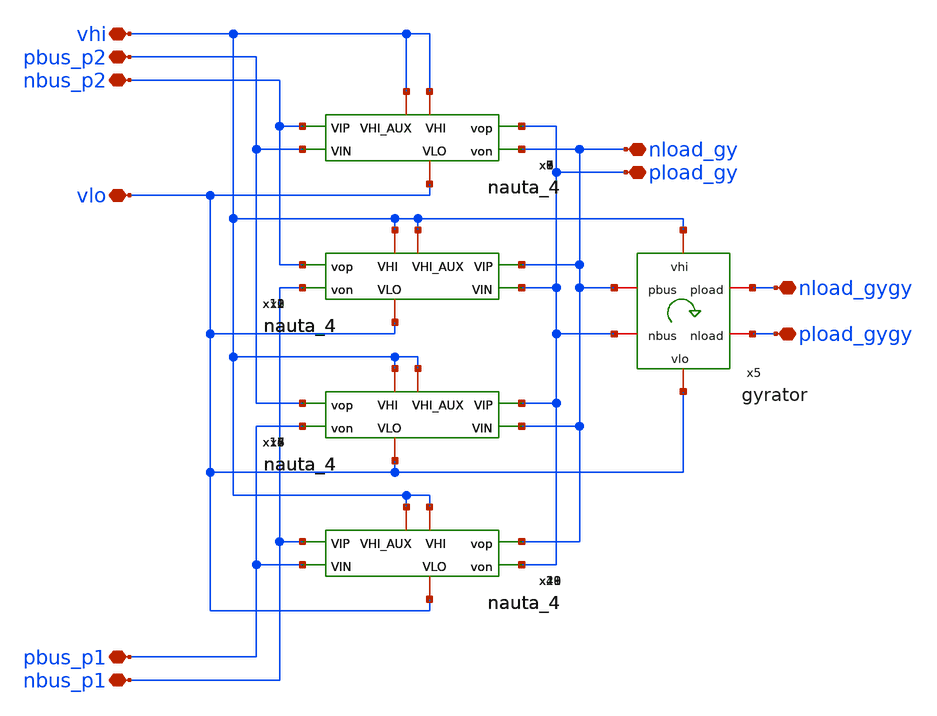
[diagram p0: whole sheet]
** sch_path: xschem/floater.sch
**.subckt floater nbus_p1 pbus_p1 nbus_p2 pbus_p2 vhi vlo pload_gy nload_gy pload_gygy nload_gygy
*.iopin nbus_p1
*.iopin pbus_p1
*.iopin nbus_p2
*.iopin pbus_p2
*.iopin vhi
*.iopin vlo
*.iopin pload_gy
*.iopin nload_gy
*.iopin pload_gygy
*.iopin nload_gygy
x1 vhi vhi nbus_p2 pload_gy pbus_p2 nload_gy vlo nauta_4
x2 vhi vhi nload_gy nbus_p2 pload_gy nbus_p1 vlo nauta_4
x3 vhi vhi pload_gy pbus_p2 nload_gy pbus_p1 vlo nauta_4
x4 vhi vhi nbus_p1 nload_gy pbus_p1 pload_gy vlo nauta_4
x5 vhi nload_gygy nload_gy pload_gygy pload_gy vlo gyrator
x6 vhi vhi nbus_p2 pload_gy pbus_p2 nload_gy vlo nauta_4
x7 vhi vhi nbus_p2 pload_gy pbus_p2 nload_gy vlo nauta_4
x8 vhi vhi nbus_p2 pload_gy pbus_p2 nload_gy vlo nauta_4
x9 vhi vhi nbus_p2 pload_gy pbus_p2 nload_gy vlo nauta_4
x10 vhi vhi nload_gy nbus_p2 pload_gy nbus_p1 vlo nauta_4
x11 vhi vhi nload_gy nbus_p2 pload_gy nbus_p1 vlo nauta_4
x12 vhi vhi nload_gy nbus_p2 pload_gy nbus_p1 vlo nauta_4
x13 vhi vhi nload_gy nbus_p2 pload_gy nbus_p1 vlo nauta_4
x14 vhi vhi pload_gy pbus_p2 nload_gy pbus_p1 vlo nauta_4
x15 vhi vhi pload_gy pbus_p2 nload_gy pbus_p1 vlo nauta_4
x16 vhi vhi pload_gy pbus_p2 nload_gy pbus_p1 vlo nauta_4
x17 vhi vhi pload_gy pbus_p2 nload_gy pbus_p1 vlo nauta_4
x18 vhi vhi nbus_p1 nload_gy pbus_p1 pload_gy vlo nauta_4
x19 vhi vhi nbus_p1 nload_gy pbus_p1 pload_gy vlo nauta_4
x20 vhi vhi nbus_p1 nload_gy pbus_p1 pload_gy vlo nauta_4
x21 vhi vhi nbus_p1 nload_gy pbus_p1 pload_gy vlo nauta_4
**.ends

* expanding   symbol:  nauta_4.sym # of pins=7
** sym_path: xschem/nauta_4.sym
** sch_path: xschem/nauta_4.sch
.subckt nauta_4 VHI_AUX VHI VIP vop VIN von VLO
*.ipin VIP
*.ipin VIN
*.opin vop
*.opin von
*.iopin VHI
*.iopin VHI_AUX
*.iopin VLO
**** begin user architecture code

.subckt NAUTA VOP VON VIP VIN VHI VHI_AUX VLO

XA0N VON VIP VLO VLO nmos_6p0 w=0.82u l=0.6u
XA0P VON VIP VHI VHI pmos_6p0 w=1.22u l=0.5u
XA1N VON VIP VLO VLO nmos_6p0 w=0.82u l=0.6u
XA1P VON VIP VHI VHI pmos_6p0 w=1.22u l=0.5u

XB0N VOP VIN VLO VLO nmos_6p0 w=0.82u l=0.6u
XB0P VOP VIN VHI VHI pmos_6p0 w=1.22u l=0.5u
XB1N VOP VIN VLO VLO nmos_6p0 w=0.82u l=0.6u
XB1P VOP VIN VHI VHI pmos_6p0 w=1.22u l=0.5u

XC0N VOP VON VLO VLO nmos_6p0 w=0.82u l=0.6u
XC0P VOP VON VHI VHI pmos_6p0 w=1.22u l=0.5u

XD0N VON VOP VLO VLO nmos_6p0 w=0.82u l=0.6u
XD0P VON VOP VHI VHI pmos_6p0 w=1.22u l=0.5u

XC1N VOP VOP VLO VLO nmos_6p0 w=0.82u l=0.6u
XC1P VOP VOP VHI_AUX VHI_AUX pmos_6p0 w=1.22u l=0.5u

XD1N VON VON VLO VLO nmos_6p0 w=0.82u l=0.6u
XD1P VON VON VHI_AUX VHI_AUX pmos_6p0 w=1.22u l=0.5u

.ends

XDUT VOP VON VIP VIN VHI VHI_AUX VLO NAUTA


**** end user architecture code
.ends


* expanding   symbol:  gyrator.sym # of pins=6
** sym_path: xschem/gyrator.sym
** sch_path: xschem/gyrator.sch
.subckt gyrator vhi pload pbus nload nbus vlo
*.iopin nbus
*.iopin pbus
*.iopin vhi
*.iopin vlo
*.iopin pload
*.iopin nload
x1 vhi vhi pbus pload nbus nload vlo nauta_4
x2 vhi vhi nload pbus pload nbus vlo nauta_4
x3 vhi vhi pbus pload nbus nload vlo nauta_4
x4 vhi vhi pbus pload nbus nload vlo nauta_4
x5 vhi vhi pbus pload nbus nload vlo nauta_4
x6 vhi vhi pbus pload nbus nload vlo nauta_4
x7 vhi vhi nload pbus pload nbus vlo nauta_4
x8 vhi vhi nload pbus pload nbus vlo nauta_4
x9 vhi vhi nload pbus pload nbus vlo nauta_4
x10 vhi vhi nload pbus pload nbus vlo nauta_4
.ends

.end
